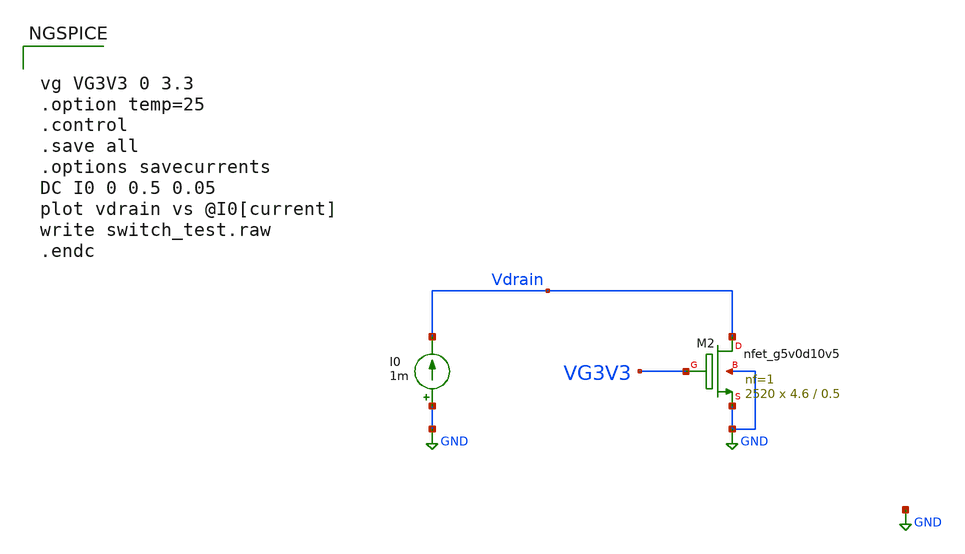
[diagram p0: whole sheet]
** sch_path: images/foss-asic-tools/addons/examples/open-pmic/characterization/switch_test_NMOS.sch
**.subckt switch_test_NMOS
I0 GND Vdrain 1m
XM2 Vdrain VG3V3 GND GND sky130_fd_pr__nfet_g5v0d10v5 L=0.5 W=4.6 nf=1 ad='int((nf+1)/2) * W/nf * 0.29'
+ as='int((nf+2)/2) * W/nf * 0.29' pd='2*int((nf+1)/2) * (W/nf + 0.29)' ps='2*int((nf+2)/2) * (W/nf + 0.29)'
+ nrd='0.29 / W' nrs='0.29 / W' sa=0 sb=0 sd=0 mult=2520 m=2520
**** begin user architecture code


vg VG3V3 0 3.3
.option temp=25
.control
.save all
.options savecurrents
DC I0 0 0.5 0.05
plot vdrain vs @I0[current]
write switch_test.raw
.endc



.include $::SKYWATER_MODELS/cells/nfet_01v8/sky130_fd_pr__nfet_01v8__tt.corner.spice
.include $::SKYWATER_MODELS/cells/nfet_01v8_lvt/sky130_fd_pr__nfet_01v8_lvt__tt.corner.spice
.include $::SKYWATER_MODELS/cells/pfet_01v8/sky130_fd_pr__pfet_01v8__tt.corner.spice
.include $::SKYWATER_MODELS/cells/nfet_03v3_nvt/sky130_fd_pr__nfet_03v3_nvt__tt.corner.spice
.include $::SKYWATER_MODELS/cells/nfet_05v0_nvt/sky130_fd_pr__nfet_05v0_nvt__tt.corner.spice
.include $::SKYWATER_MODELS/cells/esd_nfet_01v8/sky130_fd_pr__esd_nfet_01v8__tt.corner.spice
.include $::SKYWATER_MODELS/cells/pfet_01v8_lvt/sky130_fd_pr__pfet_01v8_lvt__tt.corner.spice
.include $::SKYWATER_MODELS/cells/pfet_01v8_hvt/sky130_fd_pr__pfet_01v8_hvt__tt.corner.spice
.include $::SKYWATER_MODELS/cells/esd_pfet_g5v0d10v5/sky130_fd_pr__esd_pfet_g5v0d10v5__tt.corner.spice
.include $::SKYWATER_MODELS/cells/pfet_g5v0d10v5/sky130_fd_pr__pfet_g5v0d10v5__tt.corner.spice
.include $::SKYWATER_MODELS/cells/pfet_g5v0d16v0/sky130_fd_pr__pfet_g5v0d16v0__tt.corner.spice
.include $::SKYWATER_MODELS/cells/nfet_g5v0d10v5/sky130_fd_pr__nfet_g5v0d10v5__tt.corner.spice
.include $::SKYWATER_MODELS/cells/nfet_g5v0d16v0/sky130_fd_pr__nfet_g5v0d16v0__tt_discrete.corner.spice
.include $::SKYWATER_MODELS/cells/esd_nfet_g5v0d10v5/sky130_fd_pr__esd_nfet_g5v0d10v5__tt.corner.spice
.include $::SKYWATER_MODELS/models/corners/tt/nonfet.spice
* Mismatch parameters
.include $::SKYWATER_MODELS/cells/nfet_01v8/sky130_fd_pr__nfet_01v8__mismatch.corner.spice
.include $::SKYWATER_MODELS/cells/pfet_01v8/sky130_fd_pr__pfet_01v8__mismatch.corner.spice
.include $::SKYWATER_MODELS/cells/nfet_01v8_lvt/sky130_fd_pr__nfet_01v8_lvt__mismatch.corner.spice
.include $::SKYWATER_MODELS/cells/pfet_01v8_lvt/sky130_fd_pr__pfet_01v8_lvt__mismatch.corner.spice
.include $::SKYWATER_MODELS/cells/pfet_01v8_hvt/sky130_fd_pr__pfet_01v8_hvt__mismatch.corner.spice
.include $::SKYWATER_MODELS/cells/nfet_g5v0d10v5/sky130_fd_pr__nfet_g5v0d10v5__mismatch.corner.spice
.include $::SKYWATER_MODELS/cells/pfet_g5v0d10v5/sky130_fd_pr__pfet_g5v0d10v5__mismatch.corner.spice
.include $::SKYWATER_MODELS/cells/nfet_05v0_nvt/sky130_fd_pr__nfet_05v0_nvt__mismatch.corner.spice
.include $::SKYWATER_MODELS/cells/nfet_03v3_nvt/sky130_fd_pr__nfet_03v3_nvt__mismatch.corner.spice
* Resistor$::SKYWATER_MODELS/Capacitor
.include $::SKYWATER_MODELS/models/r+c/res_typical__cap_typical.spice
.include $::SKYWATER_MODELS/models/r+c/res_typical__cap_typical__lin.spice
* Special cells
.include $::SKYWATER_MODELS/models/corners/tt/specialized_cells.spice
* All models
.include $::SKYWATER_MODELS/models/all.spice
* Corner
.include $::SKYWATER_MODELS/models/corners/tt/rf.spice

**** end user architecture code
**.ends
.GLOBAL GND
.end
